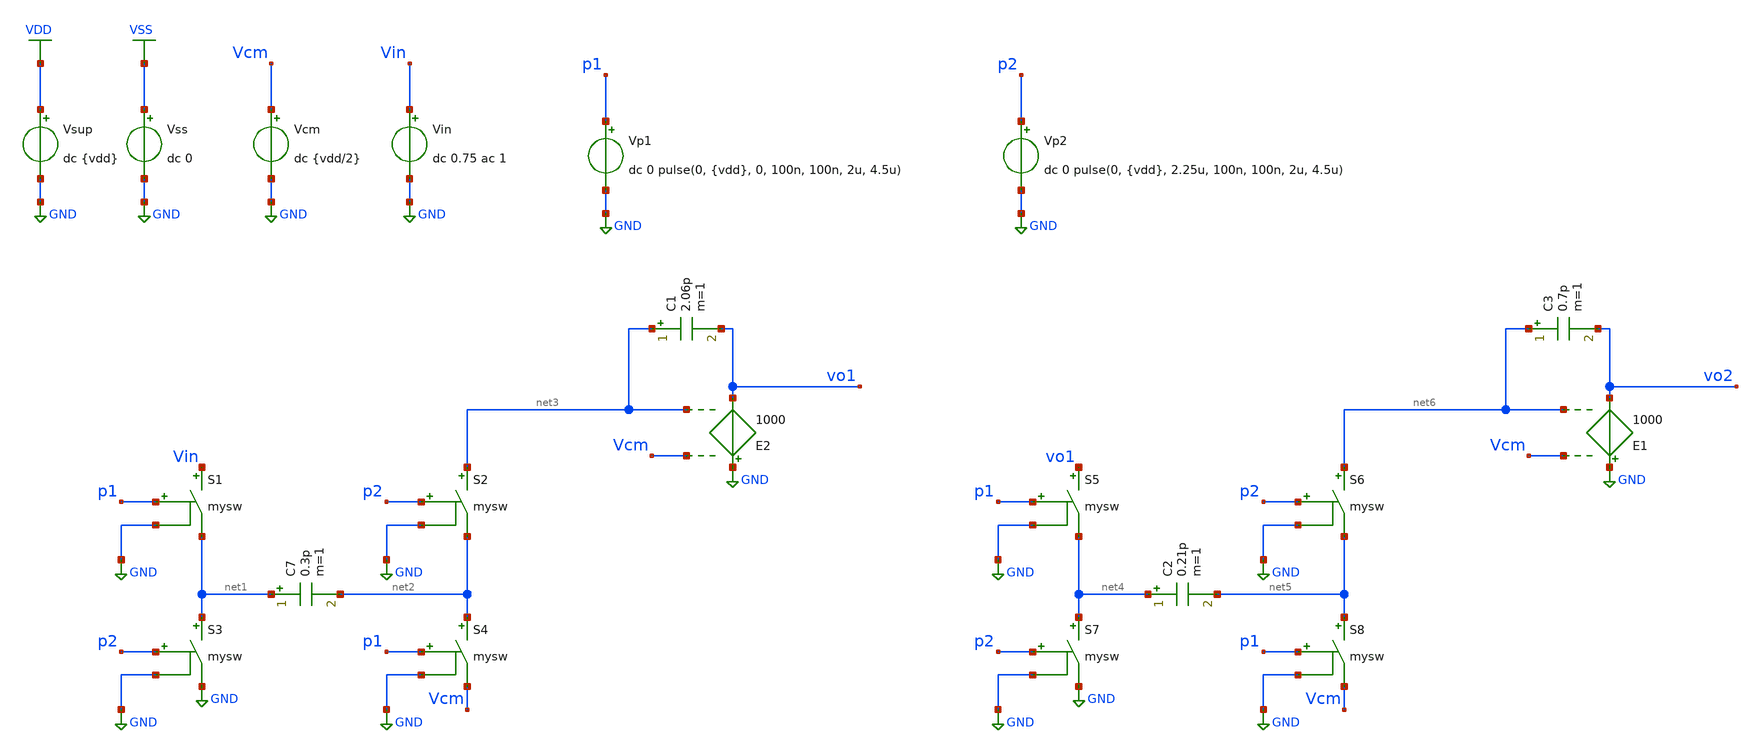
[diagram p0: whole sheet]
** sch_path: DSM/Schematics/Designs_Hrishi/IdealCircuits/IdealSwitchCapacitor_VCVS.sch
**.subckt IdealSwitchCapacitor_VCVS
Vcm Vcm GND dc {vdd/2}
Vin Vin GND dc 0.75 ac 1
S1 Vin net1 p1 GND mysw
S2 net3 net2 p2 GND mysw
S3 net1 GND p2 GND mysw
S4 net2 Vcm p1 GND mysw
C7 net1 net2 0.3p m=1
C1 net3 vo1 2.06p m=1
Vsup VDD GND dc {vdd}
Vss VSS GND dc 0
S5 vo1 net4 p1 GND mysw
S6 net6 net5 p2 GND mysw
S7 net4 GND p2 GND mysw
S8 net5 Vcm p1 GND mysw
C2 net4 net5 0.21p m=1
C3 net6 vo2 0.7p m=1
E2 GND vo1 Vcm net3 1000
E1 GND vo2 Vcm net6 1000
Vp1 p1 GND dc 0 pulse(0, {vdd}, 0, 100n, 100n, 2u, 4.5u)
Vp2 p2 GND dc 0 pulse(0, {vdd}, 2.25u, 100n, 100n, 2u, 4.5u)
**** begin user architecture code

.lib $::SG13G2_MODELS/cornerMOSlv.lib mos_tt
.lib $::SG13G2_MODELS/cornerRES.lib res_typ
.inc /foss/pdks/sg13g2/libs.ref/sg13g2_stdcell/spice/sg13g2_stdcell.spice



.param temp=27 vdd = 1.5
.model mysw SW vt={vdd/2} ron=0.1
.option method=gear reltol=1e-4

.control
save all
run
tran 40u 40u uic
plot vo1 vo2
set wr_singlescale
set wr_vecnames
wrdata IDEAL_SwitchCap.txt vo1 p1 p2
.endc


**** end user architecture code
**.ends
.GLOBAL GND
.GLOBAL VDD
.GLOBAL VSS
.end
